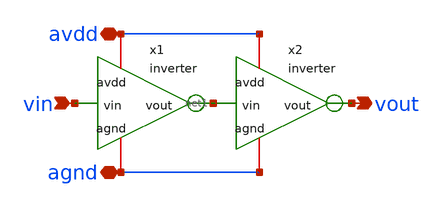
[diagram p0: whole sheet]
** sch_path: xschem/buffer.sch
**.subckt buffer avdd vin vout agnd
*.iopin avdd
*.ipin vin
*.opin vout
*.iopin agnd
x1 avdd vin net1 agnd inverter
x2 avdd net1 vout agnd inverter
**.ends

* expanding   symbol:  inverter.sym # of pins=4
** sym_path: xschem/inverter.sym
** sch_path: xschem/inverter.sch
.subckt inverter avdd vin vout agnd
*.iopin avdd
*.ipin vin
*.opin vout
*.iopin agnd
XQ1 vout base agnd agnd npn13G2 Nx=10 mm_ok=1
XR1 avdd vout sub! rhigh w=1e-6 l=0.5e-6 m=1 b=0 mm_ok=1
XR2 base vin sub! rhigh w=0.5e-6 l=0.5e-6 m=1 b=0 mm_ok=1
.ends

.end
